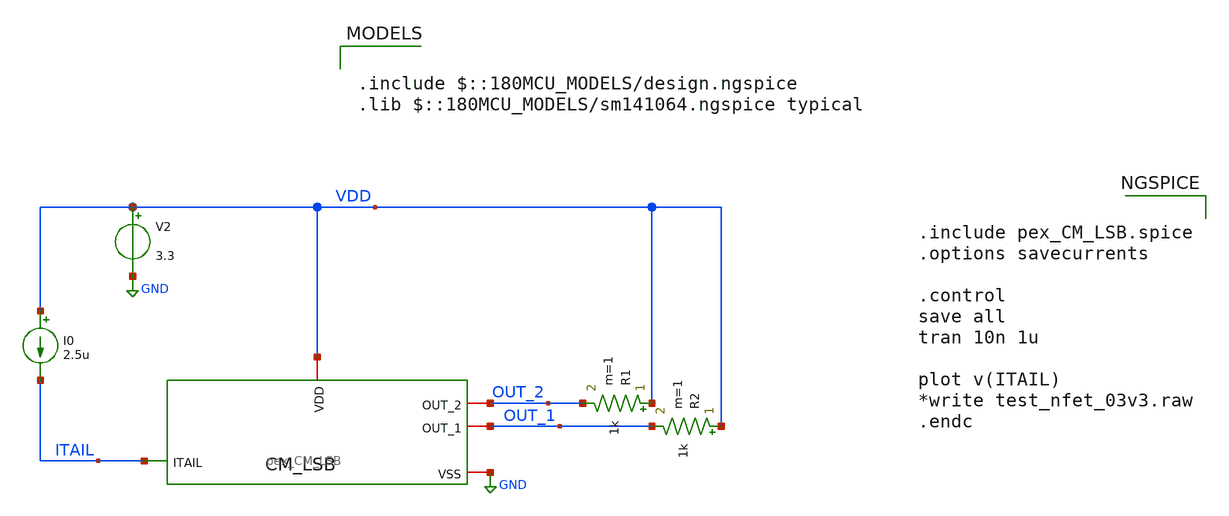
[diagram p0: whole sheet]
** sch_path: DAC_PAKISTAN_01/Pakistan1_Xschem/untitled-20.sch
**.subckt untitled-20
V2 VDD GND 3.3
I0 VDD ITAIL 2.5u
R1 VDD OUT_2 1k m=1
R2 VDD OUT_1 1k m=1
x1 ITAIL GND OUT_1 OUT_2 VDD pex_CM_LSB
**** begin user architecture code

.include $::180MCU_MODELS/design.ngspice
.lib $::180MCU_MODELS/sm141064.ngspice typical



.include pex_CM_LSB.spice
.options savecurrents

.control
save all
tran 10n 1u

plot v(ITAIL)
*write test_nfet_03v3.raw
.endc


**** end user architecture code
**.ends
.GLOBAL GND
.end
